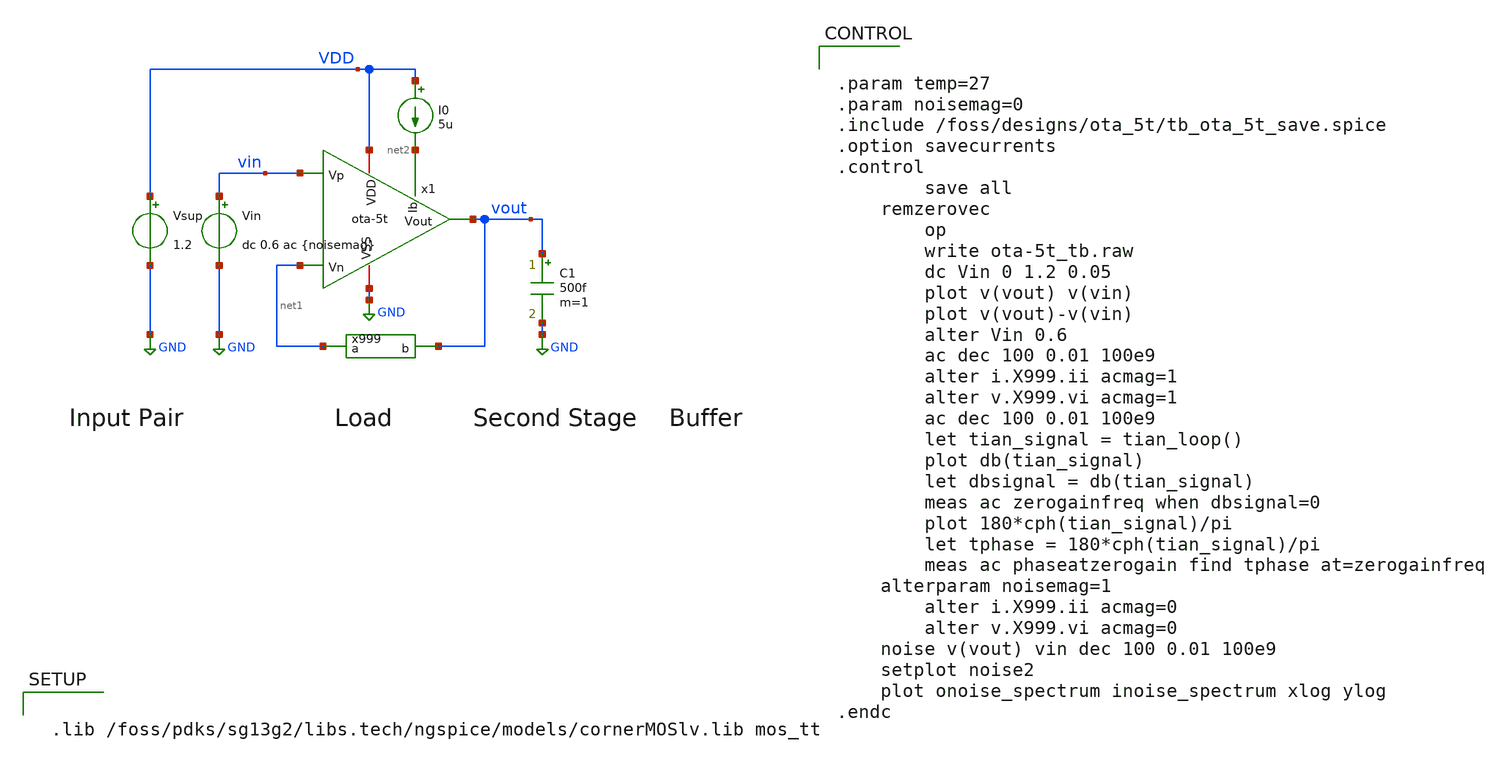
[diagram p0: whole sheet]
** sch_path: ota-5t_tb.sch
**.subckt ota-5t_tb
x1 vin net1 vout VDD GND net2 ota-5t
x999 net1 vout sub_x999
.subckt sub_x999 a b
Ii 0 x DC 0 AC 0
Vi x a DC 0 AC 1
Vnodebuffer b x 0
.ends loopgainprobe

.func tian_loop() {1/(1-1/(2*(ac1.I(v.X999.Vi)*ac2.V(X999.x)-ac1.V(X999.x)*ac2.I(v.X999.Vi))+ac1.V(X999.x)+ac2.I(v.X999.Vi)))}

C1 vout GND 500f m=1
Vin vin GND dc 0.6 ac {noisemag}
Vsup VDD GND 1.2
I0 VDD net2 5u
**** begin user architecture code


 .lib /foss/pdks/sg13g2/libs.tech/ngspice/models/cornerMOSlv.lib mos_tt




.param temp=27
.param noisemag=0
.include /foss/designs/ota_5t/tb_ota_5t_save.spice
.option savecurrents
.control
        save all
	remzerovec
        op
        write ota-5t_tb.raw
        dc Vin 0 1.2 0.05
        plot v(vout) v(vin)
        plot v(vout)-v(vin)
        alter Vin 0.6
        ac dec 100 0.01 100e9
        alter i.X999.ii acmag=1
        alter v.X999.vi acmag=1
        ac dec 100 0.01 100e9
        let tian_signal = tian_loop()
        plot db(tian_signal)
        let dbsignal = db(tian_signal)
        meas ac zerogainfreq when dbsignal=0
        plot 180*cph(tian_signal)/pi
        let tphase = 180*cph(tian_signal)/pi
        meas ac phaseatzerogain find tphase at=zerogainfreq
	alterparam noisemag=1
        alter i.X999.ii acmag=0
        alter v.X999.vi acmag=0
	noise v(vout) vin dec 100 0.01 100e9
	setplot noise2
	plot onoise_spectrum inoise_spectrum xlog ylog
.endc


**** end user architecture code
**.ends

* expanding   symbol:  /foss/designs/ota_5t/ota-5t.sym # of pins=6
** sym_path: ota-5t.sym
** sch_path: ota-5t.sch
.subckt ota-5t Vp Vn Vout VDD VSS Ib
*.iopin VDD
*.ipin Vn
*.opin Vout
*.ipin Vp
*.iopin VSS
*.ipin Ib
Xm1a vs Vn vd VSS sg13_lv_nmos w=10u l=4u ng=1 m=4 mm_ok=1
Xm2b vint vd VDD VDD sg13_lv_pmos w=2u l=2u ng=1 m=1 mm_ok=1
Xm2a vd vd VDD VDD sg13_lv_pmos w=2u l=2u ng=1 m=1 mm_ok=1
Xm3a VSS Ib vs VSS sg13_lv_nmos w=1u l=1u ng=1 m=2 mm_ok=1
Xm1b vs Vp vint VSS sg13_lv_nmos w=10u l=4u ng=1 m=4 mm_ok=1
Xm3ref VSS Ib Ib VSS sg13_lv_nmos w=1u l=1u ng=1 m=2 mm_ok=1
Xm3b VSS Ib vint2 VSS sg13_lv_nmos w=1u l=1u ng=1 m=2 mm_ok=1
Xm2c vint2 vint VDD VDD sg13_lv_pmos w=4u l=1u ng=1 m=1 mm_ok=1
Xm2d Vout vint2 VDD Vout sg13_lv_nmos w=1u l=1u ng=1 m=32 mm_ok=1
Xm3c VSS Ib Vout VSS sg13_lv_nmos w=1u l=1u ng=1 m=4 mm_ok=1
C1 vint2 net1 5p m=1
R1 net1 vint 1k m=1
.ends

.GLOBAL GND
.end
